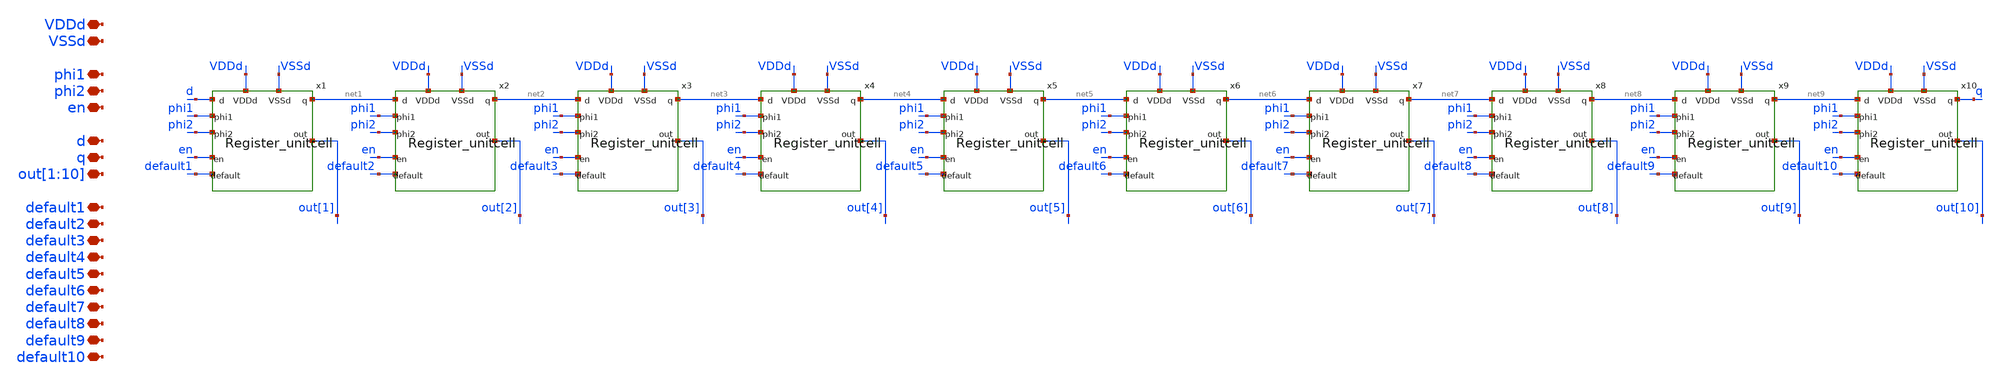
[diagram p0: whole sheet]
** sch_path: designs/libs/core_analog/SRegister_10/SRegister_10.sch
**.subckt SRegister_10 VDDd VSSd phi1 phi2 en d q
*+ out[1],out[2],out[3],out[4],out[5],out[6],out[7],out[8],out[9],out[10] default1 default2 default3 default4 default5 default6 default7 default8 default9 default10
*.iopin VDDd
*.iopin VSSd
*.iopin phi1
*.iopin phi2
*.iopin en
*.iopin d
*.iopin q
*.iopin out[1],out[2],out[3],out[4],out[5],out[6],out[7],out[8],out[9],out[10]
*.iopin default1
*.iopin default2
*.iopin default3
*.iopin default4
*.iopin default5
*.iopin default6
*.iopin default7
*.iopin default8
*.iopin default9
*.iopin default10
x1 net1 d phi1 phi2 VDDd VSSd out[1] en default1 Register_unitcell
x2 net2 net1 phi1 phi2 VDDd VSSd out[2] en default2 Register_unitcell
x3 net3 net2 phi1 phi2 VDDd VSSd out[3] en default3 Register_unitcell
x4 net4 net3 phi1 phi2 VDDd VSSd out[4] en default4 Register_unitcell
x5 net5 net4 phi1 phi2 VDDd VSSd out[5] en default5 Register_unitcell
x6 net6 net5 phi1 phi2 VDDd VSSd out[6] en default6 Register_unitcell
x7 net7 net6 phi1 phi2 VDDd VSSd out[7] en default7 Register_unitcell
x8 net8 net7 phi1 phi2 VDDd VSSd out[8] en default8 Register_unitcell
x9 net9 net8 phi1 phi2 VDDd VSSd out[9] en default9 Register_unitcell
x10 q net9 phi1 phi2 VDDd VSSd out[10] en default10 Register_unitcell
**.ends

* expanding   symbol:  libs/qw_core_analog/Register_unitcell/Register_unitcell.sym # of pins=9
** sym_path: designs/libs/qw_core_analog/Register_unitcell/Register_unitcell.sym
** sch_path: designs/libs/qw_core_analog/Register_unitcell/Register_unitcell.sch
.subckt Register_unitcell q d phi1 phi2 VDDd VSSd out en default
*.iopin phi1
*.iopin phi2
*.iopin d
*.iopin q
*.iopin en
*.iopin default
*.iopin out
*.iopin VDDd
*.iopin VSSd
x4 en VSSd VDDd VSSd VDDd enbar gf180mcu_fd_sc_mcu9t5v0__inv_1
* noconn VDDd
* noconn VSSd
x1 d q phi1 phi2 DFF_2phase_1
x2 q en VSSd VDDd VSSd VDDd or1 gf180mcu_fd_sc_mcu9t5v0__and2_1
x10 or2 or1 VSSd VDDd VSSd VDDd out gf180mcu_fd_sc_mcu9t5v0__or2_1
x3 enbar default VSSd VDDd VSSd VDDd or2 gf180mcu_fd_sc_mcu9t5v0__and2_1
.ends


* expanding   symbol:  libs/qw_core_analog/DFF_2phase_1/DFF_2phase_1.sym # of pins=4
** sym_path: designs/switch_matrix_gf180mcu_9t5v0-main/designs/libs/core_swmatrix/DFF_2phase_1.sym
** sch_path: designs/switch_matrix_gf180mcu_9t5v0-main/designs/libs/core_swmatrix/DFF_2phase_1.sch
.subckt DFF_2phase_1 D Q PHI_1 PHI_2
*.ipin D
*.ipin PHI_1
*.ipin PHI_2
*.opin Q
xmain D PHI_1 out_m VDDd VDDd VSSd VSSd gf180mcu_fd_sc_mcu9t5v0__latq_1
xsecondary out_m PHI_2 Q VDDd VDDd VSSd VSSd gf180mcu_fd_sc_mcu9t5v0__latq_1
.ends

.end
